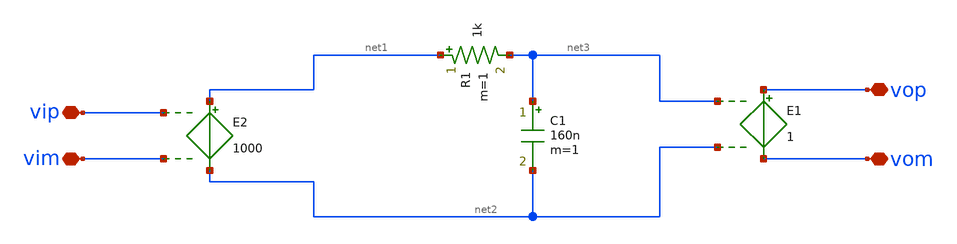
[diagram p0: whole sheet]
** sch_path: xschem/opa_mod2.sch
**.subckt opa_mod2 vip vim vop vom
*.iopin vip
*.iopin vim
*.iopin vop
*.iopin vom
E2 net1 net2 vip vim 1000
E1 vop vom net3 net2 1
R1 net1 net3 1k m=1
C1 net3 net2 160n m=1
**.ends
.end
